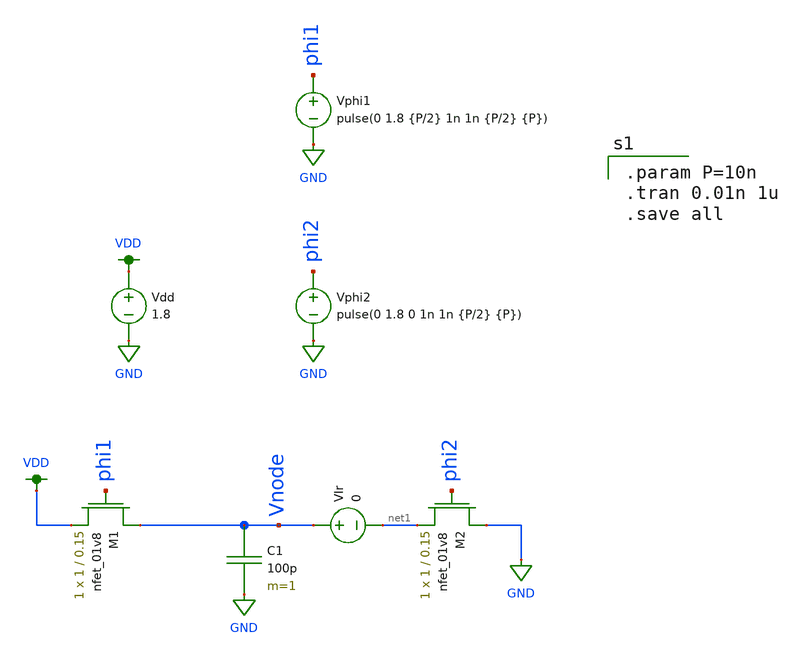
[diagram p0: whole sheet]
** sch_path: xschem/switched_capacitor/switched_capacitor_ohms_law.sch
**.subckt switched_capacitor_ohms_law
C1 Vnode GND 100p m=1
XM1 Vnode phi1 VDD GND sky130_fd_pr__nfet_01v8 L=0.15 W=1 nf=1 ad='int((nf+1)/2) * W/nf * 0.29' as='int((nf+2)/2) * W/nf * 0.29'
+ pd='2*int((nf+1)/2) * (W/nf + 0.29)' ps='2*int((nf+2)/2) * (W/nf + 0.29)' nrd='0.29 / W' nrs='0.29 / W'
+ sa=0 sb=0 sd=0 mult=1 m=1
XM2 GND phi2 net1 GND sky130_fd_pr__nfet_01v8 L=0.15 W=1 nf=1 ad='int((nf+1)/2) * W/nf * 0.29' as='int((nf+2)/2) * W/nf * 0.29'
+ pd='2*int((nf+1)/2) * (W/nf + 0.29)' ps='2*int((nf+2)/2) * (W/nf + 0.29)' nrd='0.29 / W' nrs='0.29 / W'
+ sa=0 sb=0 sd=0 mult=1 m=1
Vphi1 phi1 GND pulse(0 1.8 {P/2} 1n 1n {P/2} {P})
Vphi2 phi2 GND pulse(0 1.8 0 1n 1n {P/2} {P})
Vdd VDD GND 1.8
VIr Vnode net1 0
**** begin user architecture code

.option wnflag=1
.param MC_SWITCH=0.0
.lib ~/skywater/skywater-pdk/libraries/sky130_fd_pr_ngspice/latest/models/sky130.lib.spice tt


.param P=10n
.tran 0.01n 1u
.save all

**** end user architecture code
**.ends
.GLOBAL VDD
.GLOBAL GND
.end
